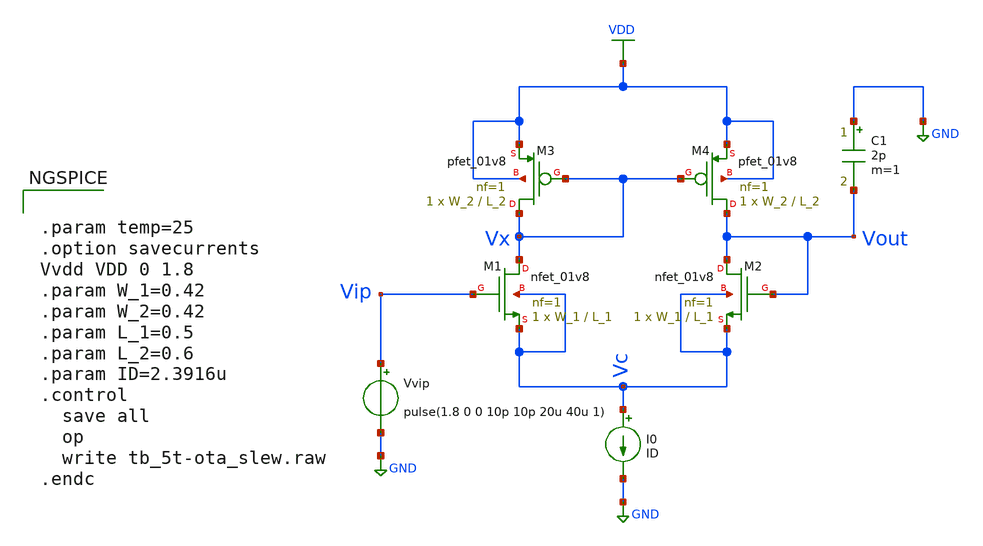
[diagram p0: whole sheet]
** sch_path: Xschem Simulations/5T-OTA/tb_5t-ota_slew.sch
**.subckt tb_5t-ota_slew
XM1 Vx Vip Vc Vc sky130_fd_pr__nfet_01v8 L=L_1 W=W_1 nf=1 ad='int((1 + 1)/2) * W_1 / 1 * 0.29' as='int((1 + 2)/2) * W_1 / 1 * 0.29'
+ pd='2*int((1 + 1)/2) * (W_1 / 1 + 0.29)' ps='2*int((1 + 2)/2) * (W_1 / 1 + 0.29)' nrd='0.29 / W_1 ' nrs='0.29 / W_1 '
+ sa=0 sb=0 sd=0 mult=1 m=1
XM2 Vout Vout Vc Vc sky130_fd_pr__nfet_01v8 L=L_1 W=W_1 nf=1 ad='int((1 + 1)/2) * W_1 / 1 * 0.29' as='int((1 + 2)/2) * W_1 / 1 * 0.29'
+ pd='2*int((1 + 1)/2) * (W_1 / 1 + 0.29)' ps='2*int((1 + 2)/2) * (W_1 / 1 + 0.29)' nrd='0.29 / W_1 ' nrs='0.29 / W_1 '
+ sa=0 sb=0 sd=0 mult=1 m=1
I0 Vc GND ID
Vvip Vip GND pulse(1.8 0 0 10p 10p 20u 40u 1)
C1 GND Vout 2p m=1
XM3 Vx Vx VDD VDD sky130_fd_pr__pfet_01v8 L=L_2 W=W_2 nf=1 ad='int((1 + 1)/2) * W_2 / 1 * 0.29' as='int((1 + 2)/2) * W_2 / 1 * 0.29'
+ pd='2*int((1 + 1)/2) * (W_2 / 1 + 0.29)' ps='2*int((1 + 2)/2) * (W_2 / 1 + 0.29)' nrd='0.29 / W_2 ' nrs='0.29 / W_2 '
+ sa=0 sb=0 sd=0 mult=1 m=1
XM4 Vout Vx VDD VDD sky130_fd_pr__pfet_01v8 L=L_2 W=W_2 nf=1 ad='int((1 + 1)/2) * W_2 / 1 * 0.29' as='int((1 + 2)/2) * W_2 / 1 * 0.29'
+ pd='2*int((1 + 1)/2) * (W_2 / 1 + 0.29)' ps='2*int((1 + 2)/2) * (W_2 / 1 + 0.29)' nrd='0.29 / W_2 ' nrs='0.29 / W_2 '
+ sa=0 sb=0 sd=0 mult=1 m=1
**** begin user architecture code

** opencircuitdesign pdks install
.lib $::SKYWATER_MODELS/sky130.lib.spice tt



.param temp=25
.option savecurrents
Vvdd VDD 0 1.8
.param W_1=0.42
.param W_2=0.42
.param L_1=0.5
.param L_2=0.6
.param ID=2.3916u
.control
  save all
  op
  write tb_5t-ota_slew.raw
.endc




.control
  tran 10n 30u 10u
  save all

  plot v(vip) v(vout)

  meas tran v_max FIND v(vout) AT=29u
  meas tran v_min FIND v(vout) AT=11u

  let v10 = v_min + (0.1*(v_max-v_min))
  let v90 = v_max - (0.1*(v_max-v_min))
  meas tran t10 WHEN v(vout)=v10 RISE=1
  meas tran t90 WHEN v(vout)=v90 RISE=1

  let slew_rate = ((v90 - v10) / (t90 - t10)) * 1e-6
  print slew_rate
.endc


**** end user architecture code
**.ends
.GLOBAL GND
.GLOBAL VDD
.end
